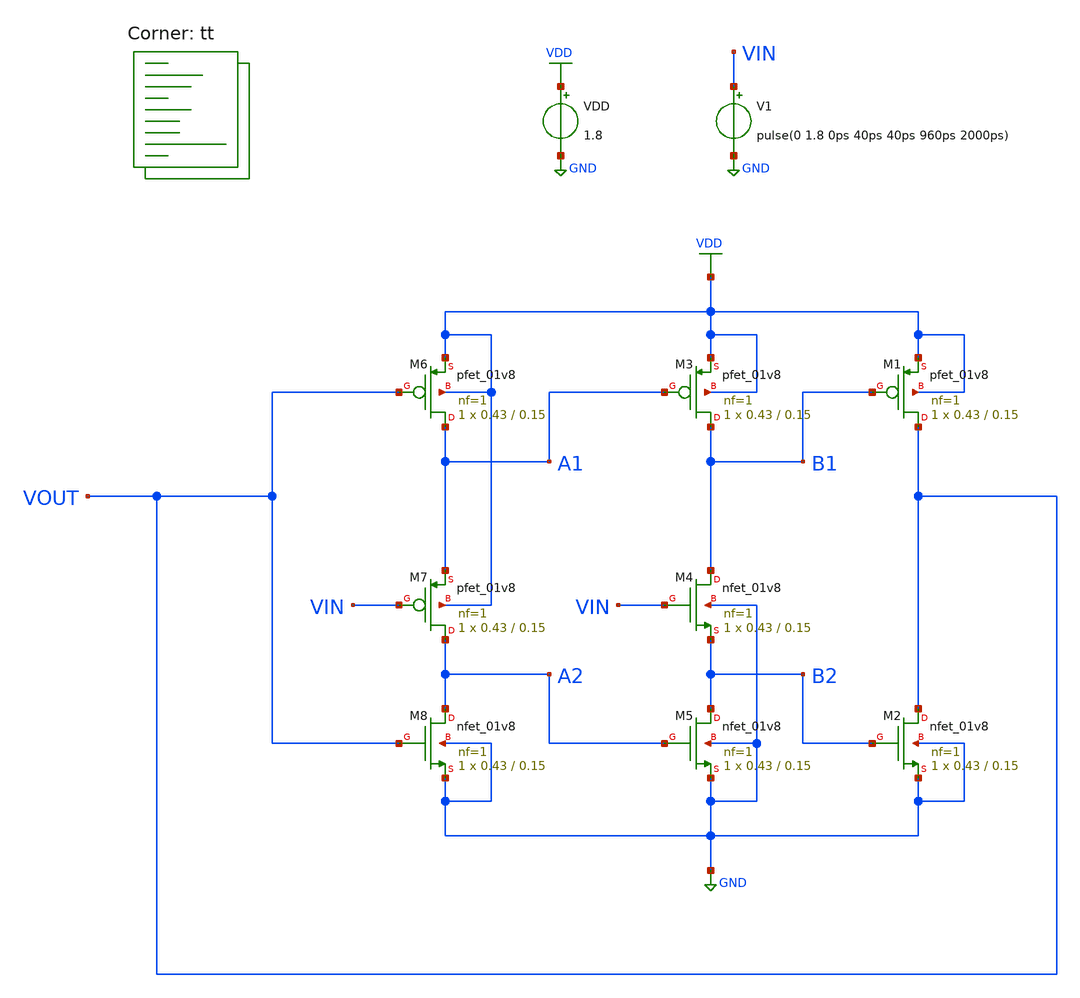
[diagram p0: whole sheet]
** sch_path: projects/pll/divider/xschem_ngspice/tb_TSPC_FF_split_path_3.sch
**.subckt tb_TSPC_FF_split_path_3
VDD VDD GND 1.8
V1 VIN GND pulse(0 1.8 0ps 40ps 40ps 960ps 2000ps)
XM1 VOUT B1 VDD VDD sky130_fd_pr__pfet_01v8 L=0.15 W=0.43 nf=1 ad='int((nf+1)/2) * W/nf * 0.29' as='int((nf+2)/2) * W/nf * 0.29'
+ pd='2*int((nf+1)/2) * (W/nf + 0.29)' ps='2*int((nf+2)/2) * (W/nf + 0.29)' nrd='0.29 / W' nrs='0.29 / W'
+ sa=0 sb=0 sd=0 mult=1 m=1
XM4 B1 VIN B2 GND sky130_fd_pr__nfet_01v8 L=0.15 W=0.43 nf=1 ad='int((nf+1)/2) * W/nf * 0.29' as='int((nf+2)/2) * W/nf * 0.29'
+ pd='2*int((nf+1)/2) * (W/nf + 0.29)' ps='2*int((nf+2)/2) * (W/nf + 0.29)' nrd='0.29 / W' nrs='0.29 / W'
+ sa=0 sb=0 sd=0 mult=1 m=1
XM2 VOUT B2 GND GND sky130_fd_pr__nfet_01v8 L=0.15 W=0.43 nf=1 ad='int((nf+1)/2) * W/nf * 0.29' as='int((nf+2)/2) * W/nf * 0.29'
+ pd='2*int((nf+1)/2) * (W/nf + 0.29)' ps='2*int((nf+2)/2) * (W/nf + 0.29)' nrd='0.29 / W' nrs='0.29 / W'
+ sa=0 sb=0 sd=0 mult=1 m=1
XM3 B1 A1 VDD VDD sky130_fd_pr__pfet_01v8 L=0.15 W=0.43 nf=1 ad='int((nf+1)/2) * W/nf * 0.29' as='int((nf+2)/2) * W/nf * 0.29'
+ pd='2*int((nf+1)/2) * (W/nf + 0.29)' ps='2*int((nf+2)/2) * (W/nf + 0.29)' nrd='0.29 / W' nrs='0.29 / W'
+ sa=0 sb=0 sd=0 mult=1 m=1
XM5 B2 A2 GND GND sky130_fd_pr__nfet_01v8 L=0.15 W=0.43 nf=1 ad='int((nf+1)/2) * W/nf * 0.29' as='int((nf+2)/2) * W/nf * 0.29'
+ pd='2*int((nf+1)/2) * (W/nf + 0.29)' ps='2*int((nf+2)/2) * (W/nf + 0.29)' nrd='0.29 / W' nrs='0.29 / W'
+ sa=0 sb=0 sd=0 mult=1 m=1
XM6 A1 VOUT VDD VDD sky130_fd_pr__pfet_01v8 L=0.15 W=0.43 nf=1 ad='int((nf+1)/2) * W/nf * 0.29' as='int((nf+2)/2) * W/nf * 0.29'
+ pd='2*int((nf+1)/2) * (W/nf + 0.29)' ps='2*int((nf+2)/2) * (W/nf + 0.29)' nrd='0.29 / W' nrs='0.29 / W'
+ sa=0 sb=0 sd=0 mult=1 m=1
XM8 A2 VOUT GND GND sky130_fd_pr__nfet_01v8 L=0.15 W=0.43 nf=1 ad='int((nf+1)/2) * W/nf * 0.29' as='int((nf+2)/2) * W/nf * 0.29'
+ pd='2*int((nf+1)/2) * (W/nf + 0.29)' ps='2*int((nf+2)/2) * (W/nf + 0.29)' nrd='0.29 / W' nrs='0.29 / W'
+ sa=0 sb=0 sd=0 mult=1 m=1
XM7 A2 VIN A1 VDD sky130_fd_pr__pfet_01v8 L=0.15 W=0.43 nf=1 ad='int((nf+1)/2) * W/nf * 0.29' as='int((nf+2)/2) * W/nf * 0.29'
+ pd='2*int((nf+1)/2) * (W/nf + 0.29)' ps='2*int((nf+2)/2) * (W/nf + 0.29)' nrd='0.29 / W' nrs='0.29 / W'
+ sa=0 sb=0 sd=0 mult=1 m=1
**** begin user architecture code



.include /foss/pdks/sky130A/libs.ref/sky130_fd_sc_hd/spice/sky130_fd_sc_hd.spice

.option method=gear
.option wnflag=1
.option savecurrents


*.ic v(d)=0
*.ic v(q)=0
*.ic v(q1)=0

* .probe p(x1)

.control

*  save v(vin) v(vout) p(x1:power)
  save all
  * save all
  * tran 0.1n 1u
  tran 0.05p 10n

  remzerovec
  write tb_TSPC_FF_split_path_3.raw
  * set appendwrite

.endc



.lib $::SKYWATER_MODELS/sky130.lib.spice tt
**** end user architecture code
**.ends
.GLOBAL GND
.GLOBAL VDD
.end
